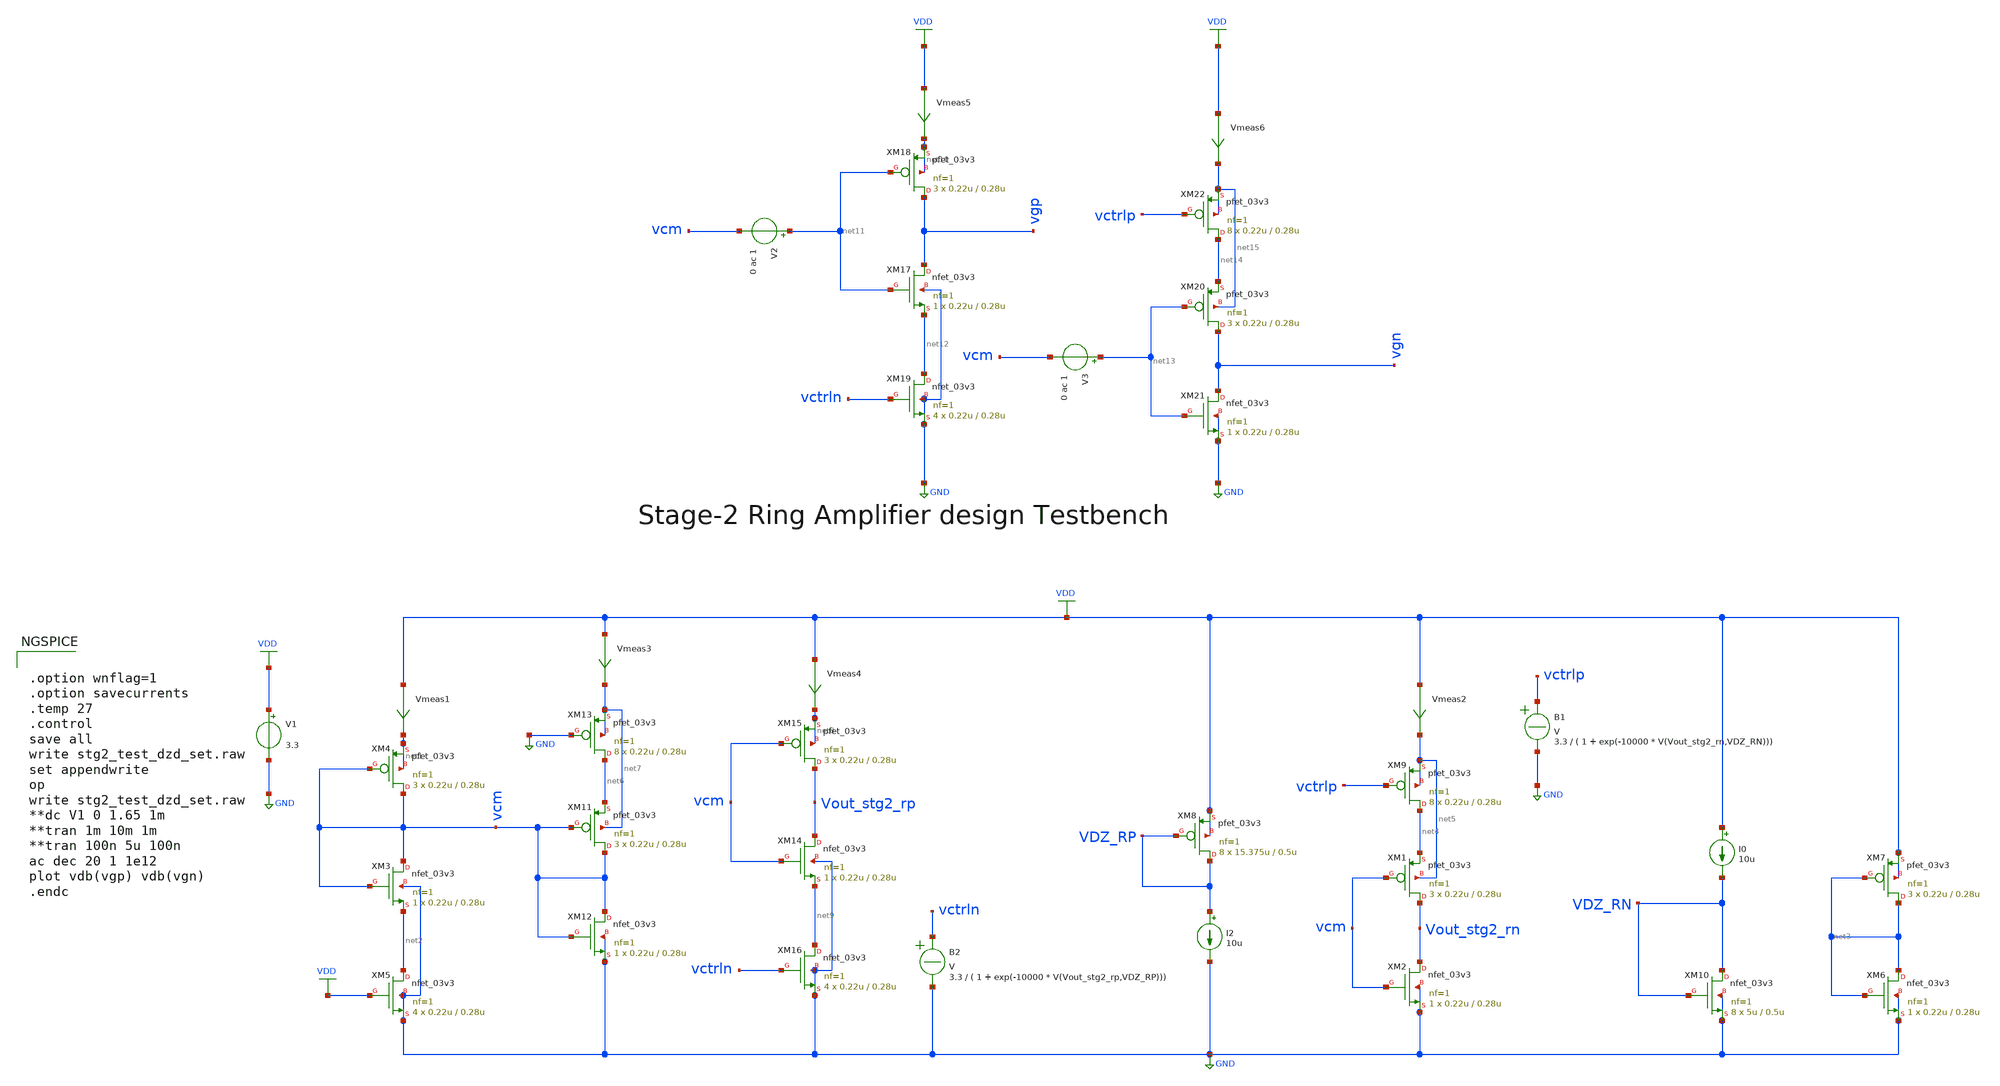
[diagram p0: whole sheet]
** sch_path: Design_Files/Ring-amp/STG2/stg2_test_dzd_set.sch
**.subckt stg2_test_dzd_set
XM3 vcm vcm net2 GND nfet_03v3 L=0.28u W=0.22u nf=1 ad='int((nf+1)/2) * W/nf * 0.18u' as='int((nf+2)/2) * W/nf * 0.18u'
+ pd='2*int((nf+1)/2) * (W/nf + 0.18u)' ps='2*int((nf+2)/2) * (W/nf + 0.18u)' nrd='0.18u / W' nrs='0.18u / W'
+ sa=0 sb=0 sd=0 m=1
XM4 vcm vcm net1 net1 pfet_03v3 L=0.28u W=0.22u nf=1 ad='int((nf+1)/2) * W/nf * 0.18u' as='int((nf+2)/2) * W/nf * 0.18u'
+ pd='2*int((nf+1)/2) * (W/nf + 0.18u)' ps='2*int((nf+2)/2) * (W/nf + 0.18u)' nrd='0.18u / W' nrs='0.18u / W'
+ sa=0 sb=0 sd=0 m=3
XM5 net2 VDD GND GND nfet_03v3 L=0.28u W=0.22u nf=1 ad='int((nf+1)/2) * W/nf * 0.18u' as='int((nf+2)/2) * W/nf * 0.18u'
+ pd='2*int((nf+1)/2) * (W/nf + 0.18u)' ps='2*int((nf+2)/2) * (W/nf + 0.18u)' nrd='0.18u / W' nrs='0.18u / W'
+ sa=0 sb=0 sd=0 m=4
XM6 net3 net3 GND GND nfet_03v3 L=0.28u W=0.22u nf=1 ad='int((nf+1)/2) * W/nf * 0.18u' as='int((nf+2)/2) * W/nf * 0.18u'
+ pd='2*int((nf+1)/2) * (W/nf + 0.18u)' ps='2*int((nf+2)/2) * (W/nf + 0.18u)' nrd='0.18u / W' nrs='0.18u / W'
+ sa=0 sb=0 sd=0 m=1
XM7 net3 net3 VDD VDD pfet_03v3 L=0.28u W=0.22u nf=1 ad='int((nf+1)/2) * W/nf * 0.18u' as='int((nf+2)/2) * W/nf * 0.18u'
+ pd='2*int((nf+1)/2) * (W/nf + 0.18u)' ps='2*int((nf+2)/2) * (W/nf + 0.18u)' nrd='0.18u / W' nrs='0.18u / W'
+ sa=0 sb=0 sd=0 m=3
XM8 VDZ_RP VDZ_RP VDD VDD pfet_03v3 L=0.5u W=15.375u nf=1 ad='int((nf+1)/2) * W/nf * 0.18u' as='int((nf+2)/2) * W/nf * 0.18u'
+ pd='2*int((nf+1)/2) * (W/nf + 0.18u)' ps='2*int((nf+2)/2) * (W/nf + 0.18u)' nrd='0.18u / W' nrs='0.18u / W'
+ sa=0 sb=0 sd=0 m=8
I2 VDZ_RP GND 10u
B2 vctrln GND V = 3.3 / ( 1 + exp(-10000 * V(Vout_stg2_rp,VDZ_RP)))
V1 VDD GND 3.3
Vmeas1 VDD net1 0
.save i(vmeas1)
XM1 Vout_stg2_rn vcm net4 net5 pfet_03v3 L=0.28u W=0.22u nf=1 ad='int((nf+1)/2) * W/nf * 0.18u' as='int((nf+2)/2) * W/nf * 0.18u'
+ pd='2*int((nf+1)/2) * (W/nf + 0.18u)' ps='2*int((nf+2)/2) * (W/nf + 0.18u)' nrd='0.18u / W' nrs='0.18u / W'
+ sa=0 sb=0 sd=0 m=3
XM2 Vout_stg2_rn vcm GND GND nfet_03v3 L=0.28u W=0.22u nf=1 ad='int((nf+1)/2) * W/nf * 0.18u' as='int((nf+2)/2) * W/nf * 0.18u'
+ pd='2*int((nf+1)/2) * (W/nf + 0.18u)' ps='2*int((nf+2)/2) * (W/nf + 0.18u)' nrd='0.18u / W' nrs='0.18u / W'
+ sa=0 sb=0 sd=0 m=1
XM9 net4 vctrlp net5 net5 pfet_03v3 L=0.28u W=0.22u nf=1 ad='int((nf+1)/2) * W/nf * 0.18u' as='int((nf+2)/2) * W/nf * 0.18u'
+ pd='2*int((nf+1)/2) * (W/nf + 0.18u)' ps='2*int((nf+2)/2) * (W/nf + 0.18u)' nrd='0.18u / W' nrs='0.18u / W'
+ sa=0 sb=0 sd=0 m=8
Vmeas2 VDD net5 0
.save i(vmeas2)
XM10 VDZ_RN VDZ_RN GND GND nfet_03v3 L=0.5u W=5u nf=1 ad='int((nf+1)/2) * W/nf * 0.18u' as='int((nf+2)/2) * W/nf * 0.18u'
+ pd='2*int((nf+1)/2) * (W/nf + 0.18u)' ps='2*int((nf+2)/2) * (W/nf + 0.18u)' nrd='0.18u / W' nrs='0.18u / W'
+ sa=0 sb=0 sd=0 m=8
I0 VDD VDZ_RN 10u
B1 vctrlp GND V = 3.3 / ( 1 + exp(-10000 * V(Vout_stg2_rn,VDZ_RN)))
XM11 vcm vcm net6 net7 pfet_03v3 L=0.28u W=0.22u nf=1 ad='int((nf+1)/2) * W/nf * 0.18u' as='int((nf+2)/2) * W/nf * 0.18u'
+ pd='2*int((nf+1)/2) * (W/nf + 0.18u)' ps='2*int((nf+2)/2) * (W/nf + 0.18u)' nrd='0.18u / W' nrs='0.18u / W'
+ sa=0 sb=0 sd=0 m=3
XM12 vcm vcm GND GND nfet_03v3 L=0.28u W=0.22u nf=1 ad='int((nf+1)/2) * W/nf * 0.18u' as='int((nf+2)/2) * W/nf * 0.18u'
+ pd='2*int((nf+1)/2) * (W/nf + 0.18u)' ps='2*int((nf+2)/2) * (W/nf + 0.18u)' nrd='0.18u / W' nrs='0.18u / W'
+ sa=0 sb=0 sd=0 m=1
XM13 net6 GND net7 net7 pfet_03v3 L=0.28u W=0.22u nf=1 ad='int((nf+1)/2) * W/nf * 0.18u' as='int((nf+2)/2) * W/nf * 0.18u'
+ pd='2*int((nf+1)/2) * (W/nf + 0.18u)' ps='2*int((nf+2)/2) * (W/nf + 0.18u)' nrd='0.18u / W' nrs='0.18u / W'
+ sa=0 sb=0 sd=0 m=8
Vmeas3 VDD net7 0
.save i(vmeas3)
XM14 Vout_stg2_rp vcm net9 GND nfet_03v3 L=0.28u W=0.22u nf=1 ad='int((nf+1)/2) * W/nf * 0.18u' as='int((nf+2)/2) * W/nf * 0.18u'
+ pd='2*int((nf+1)/2) * (W/nf + 0.18u)' ps='2*int((nf+2)/2) * (W/nf + 0.18u)' nrd='0.18u / W' nrs='0.18u / W'
+ sa=0 sb=0 sd=0 m=1
XM15 Vout_stg2_rp vcm net8 net8 pfet_03v3 L=0.28u W=0.22u nf=1 ad='int((nf+1)/2) * W/nf * 0.18u' as='int((nf+2)/2) * W/nf * 0.18u'
+ pd='2*int((nf+1)/2) * (W/nf + 0.18u)' ps='2*int((nf+2)/2) * (W/nf + 0.18u)' nrd='0.18u / W' nrs='0.18u / W'
+ sa=0 sb=0 sd=0 m=3
XM16 net9 vctrln GND GND nfet_03v3 L=0.28u W=0.22u nf=1 ad='int((nf+1)/2) * W/nf * 0.18u' as='int((nf+2)/2) * W/nf * 0.18u'
+ pd='2*int((nf+1)/2) * (W/nf + 0.18u)' ps='2*int((nf+2)/2) * (W/nf + 0.18u)' nrd='0.18u / W' nrs='0.18u / W'
+ sa=0 sb=0 sd=0 m=4
Vmeas4 VDD net8 0
.save i(vmeas4)
XM17 vgp net11 net12 GND nfet_03v3 L=0.28u W=0.22u nf=1 ad='int((nf+1)/2) * W/nf * 0.18u' as='int((nf+2)/2) * W/nf * 0.18u'
+ pd='2*int((nf+1)/2) * (W/nf + 0.18u)' ps='2*int((nf+2)/2) * (W/nf + 0.18u)' nrd='0.18u / W' nrs='0.18u / W'
+ sa=0 sb=0 sd=0 m=1
XM18 vgp net11 net10 net10 pfet_03v3 L=0.28u W=0.22u nf=1 ad='int((nf+1)/2) * W/nf * 0.18u' as='int((nf+2)/2) * W/nf * 0.18u'
+ pd='2*int((nf+1)/2) * (W/nf + 0.18u)' ps='2*int((nf+2)/2) * (W/nf + 0.18u)' nrd='0.18u / W' nrs='0.18u / W'
+ sa=0 sb=0 sd=0 m=3
XM19 net12 vctrln GND GND nfet_03v3 L=0.28u W=0.22u nf=1 ad='int((nf+1)/2) * W/nf * 0.18u' as='int((nf+2)/2) * W/nf * 0.18u'
+ pd='2*int((nf+1)/2) * (W/nf + 0.18u)' ps='2*int((nf+2)/2) * (W/nf + 0.18u)' nrd='0.18u / W' nrs='0.18u / W'
+ sa=0 sb=0 sd=0 m=4
Vmeas5 VDD net10 0
.save i(vmeas5)
V2 net11 vcm 0 ac 1
XM20 vgn net13 net14 net15 pfet_03v3 L=0.28u W=0.22u nf=1 ad='int((nf+1)/2) * W/nf * 0.18u' as='int((nf+2)/2) * W/nf * 0.18u'
+ pd='2*int((nf+1)/2) * (W/nf + 0.18u)' ps='2*int((nf+2)/2) * (W/nf + 0.18u)' nrd='0.18u / W' nrs='0.18u / W'
+ sa=0 sb=0 sd=0 m=3
XM21 vgn net13 GND GND nfet_03v3 L=0.28u W=0.22u nf=1 ad='int((nf+1)/2) * W/nf * 0.18u' as='int((nf+2)/2) * W/nf * 0.18u'
+ pd='2*int((nf+1)/2) * (W/nf + 0.18u)' ps='2*int((nf+2)/2) * (W/nf + 0.18u)' nrd='0.18u / W' nrs='0.18u / W'
+ sa=0 sb=0 sd=0 m=1
XM22 net14 vctrlp net15 net15 pfet_03v3 L=0.28u W=0.22u nf=1 ad='int((nf+1)/2) * W/nf * 0.18u' as='int((nf+2)/2) * W/nf * 0.18u'
+ pd='2*int((nf+1)/2) * (W/nf + 0.18u)' ps='2*int((nf+2)/2) * (W/nf + 0.18u)' nrd='0.18u / W' nrs='0.18u / W'
+ sa=0 sb=0 sd=0 m=8
Vmeas6 VDD net15 0
.save i(vmeas6)
V3 net13 vcm 0 ac 1
**** begin user architecture code


.option wnflag=1
.option savecurrents
.temp 27
.control
save all
write stg2_test_dzd_set.raw
set appendwrite
op
write stg2_test_dzd_set.raw
**dc V1 0 1.65 1m
**tran 1m 10m 1m
**tran 100n 5u 100n
ac dec 20 1 1e12
plot vdb(vgp) vdb(vgn)
.endc



.lib /foss/pdks/volare/gf180mcu/versions/0fe599b2afb6708d281543108caf8310912f54af/gf180mcuD/libs.tech/ngspice/sm141064.ngspice typical
.include /foss/pdks/volare/gf180mcu/versions/0fe599b2afb6708d281543108caf8310912f54af/gf180mcuD/libs.tech/ngspice/design.ngspice
.lib /foss/pdks/volare/gf180mcu/versions/0fe599b2afb6708d281543108caf8310912f54af/gf180mcuD/libs.tech/ngspice/sm141064.ngspice res_statistical

**.include $::180MCU_MODELS/design.ngspice
**.lib $::180MCU_MODELS/sm141064.ngspice typical
**.lib $::180MCU_MODELS/sm141064.ngspice res_typical
* .lib $::180MCU_MODELS/sm141064.ngspice res_statistical
*.include $::180MCU_MODELS/design.ngspice
*.lib $::180MCU_MODELS/sm141064.ngspice typical




.save @m.xm1.m0[gm]
.save @m.xm1.m0[id]
.save @m.xm1.m0[vth]
.save @m.xm1.m0[gds]
.save @m.xm1.m0[cgg]
.save @m.xm1.m0[cgs]
.save @m.xm1.m0[cgd]
.save @m.xm2.m0[gm]
.save @m.xm2.m0[id]
.save @m.xm2.m0[vth]
.save @m.xm2.m0[gds]
.save @m.xm2.m0[cgg]
.save @m.xm2.m0[cgs]
.save @m.xm2.m0[cgd]
.save @m.xm3.m0[gm]
.save @m.xm3.m0[id]
.save @m.xm3.m0[vth]
.save @m.xm3.m0[vds]
.save @m.xm3.m0[gds]
.save @m.xm3.m0[cgg]
.save @m.xm3.m0[cgs]
.save @m.xm3.m0[cgd]
.save @m.xm4.m0[gm]
.save @m.xm4.m0[id]
.save @m.xm4.m0[vth]
.save @m.xm4.m0[vds]
.save @m.xm4.m0[gds]
.save @m.xm4.m0[cgg]
.save @m.xm4.m0[cgs]
.save @m.xm4.m0[cgd]


**** end user architecture code
**.ends
.GLOBAL GND
.GLOBAL VDD
.end
